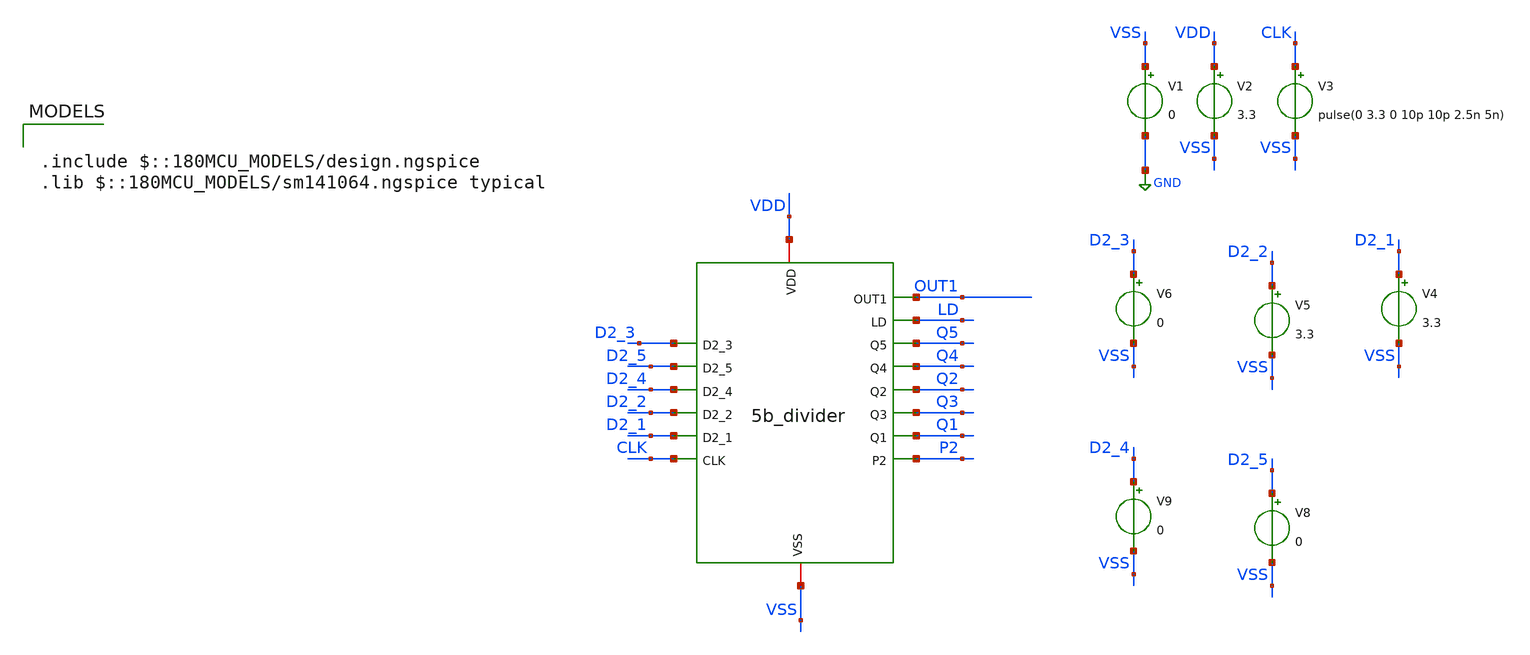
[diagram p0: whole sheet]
** sch_path: Clock_Generator_PAKISTAN_06/Schematics/5b_divider_TB.sch
**.subckt 5b_divider_TB
x1 OUT1 VDD LD D2_3 Q5 D2_5 Q4 D2_4 Q2 D2_2 Q3 D2_1 Q1 CLK P2 VSS 5b_divider
V1 VSS GND 0
V2 VDD VSS 3.3
V3 CLK VSS pulse(0 3.3 0 10p 10p 2.5n 5n)
V4 D2_1 VSS 3.3
V5 D2_2 VSS 3.3
V6 D2_3 VSS 0
V8 D2_5 VSS 0
V9 D2_4 VSS 0
**** begin user architecture code

.include $::180MCU_MODELS/design.ngspice
.lib $::180MCU_MODELS/sm141064.ngspice typical



.option savecurrents
.control
save all

tran 10n 100n
set xbrushwidth=2
set xfontsize=3
plot v(CLK) v(x1.P1)+3.5 v(x1.OUT2)+7 v(x1.P3)+10.5 v(Q3)+14 v(Q2)+17.5 v(Q1)+21 v(LD)+24.5
plot v(LD)
plot v(Q1)
plot v(Q2)
plot v(Q3) v(Q2) v(Q1)
plot v(Q4)
plot v(OUT1)
write test 3b_divider_tb.raw
write test_nfet_03v3.raw
.endc


**** end user architecture code
**.ends
.GLOBAL GND
.end
